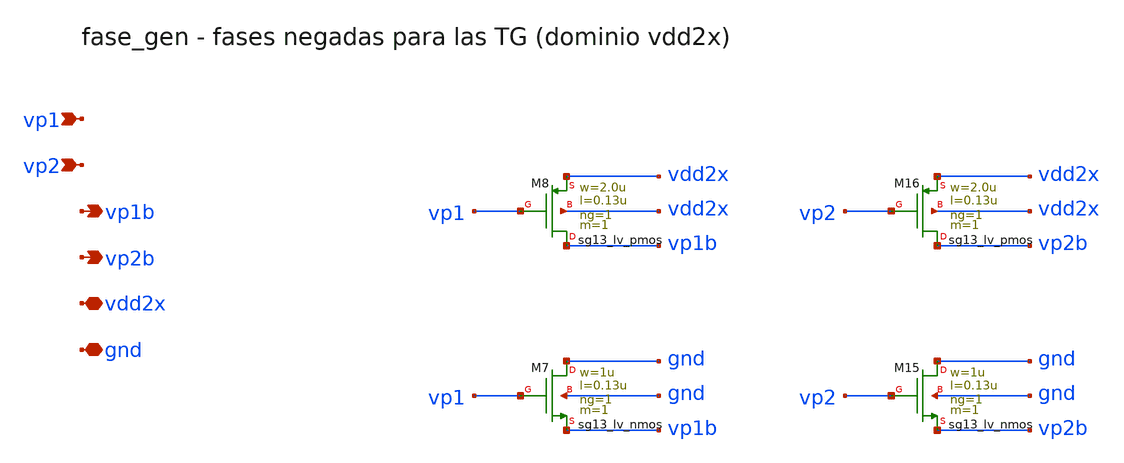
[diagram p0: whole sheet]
** sch_path: Enfoque_A/xschem/celdas/fase_gen.sch
**.subckt fase_gen vp1 vp2 vp1b vp2b vdd2x gnd
*.ipin vp1
*.ipin vp2
*.opin vp1b
*.opin vp2b
*.iopin vdd2x
*.iopin gnd
XM8 vp1b vp1 vdd2x vdd2x sg13_lv_pmos w=2.0u l=0.13u ng=1 m=1 mm_ok=1
XM7 gnd vp1 vp1b gnd sg13_lv_nmos w=1u l=0.13u ng=1 m=1 mm_ok=1
XM16 vp2b vp2 vdd2x vdd2x sg13_lv_pmos w=2.0u l=0.13u ng=1 m=1 mm_ok=1
XM15 gnd vp2 vp2b gnd sg13_lv_nmos w=1u l=0.13u ng=1 m=1 mm_ok=1
**.ends
.end
